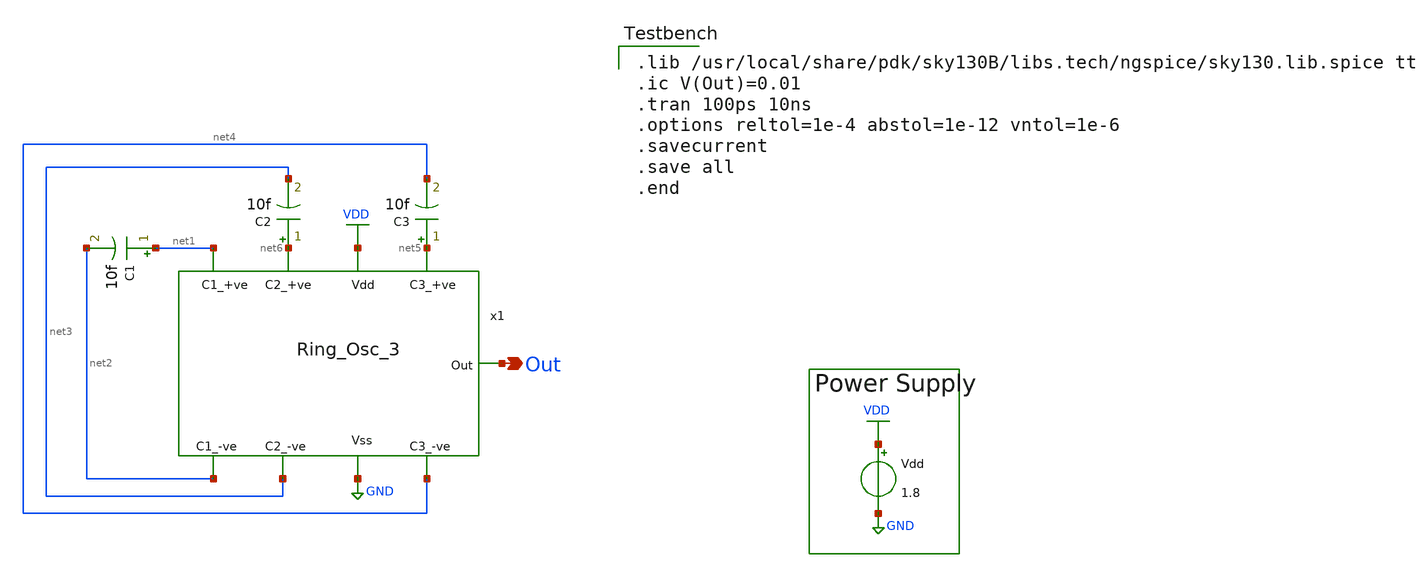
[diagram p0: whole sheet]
** sch_path: Xschem/RO_3_test.sch
**.subckt RO_3_test Out
*.opin Out
x1 VDD Out net5 net6 net1 net3 net4 net2 GND Ring_Osc_3
C1 net1 net2 10f m=1
C2 net6 net3 10f m=1
C3 net5 net4 10f m=1
Vdd VDD GND 1.8
**** begin user architecture code

.lib /usr/local/share/pdk/sky130B/libs.tech/ngspice/sky130.lib.spice tt
.ic V(Out)=0.01
.tran 100ps 10ns
.options reltol=1e-4 abstol=1e-12 vntol=1e-6
.savecurrent
.save all
.end

**** end user architecture code
**.ends

* expanding   symbol:  Ring_Osc_3.sym # of pins=9
** sym_path: Xschem/Ring_Osc_3.sym
** sch_path: Xschem/Ring_Osc_3.sch
.subckt Ring_Osc_3 Vdd Out C3_+ve C2_+ve C1_+ve C2_-ve C3_-ve C1_-ve Vss
*.opin Out
*.ipin Vss
*.ipin Vdd
*.ipin C1_-ve
*.ipin C1_+ve
*.ipin C2_-ve
*.ipin C2_+ve
*.ipin C3_+ve
*.ipin C3_-ve
x1 Vdd Out C1_+ve Vss inv
x2 Vdd C1_+ve C2_+ve Vss inv
x3 Vdd C2_+ve Out Vss inv
.ends


* expanding   symbol:  inv.sym # of pins=4
** sym_path: Xschem/inv.sym
** sch_path: Xschem/inv.sch
.subckt inv Vdd Vin Vout Vss
*.ipin Vin
*.ipin Vss
*.ipin Vdd
*.opin Vout
XM1 Vout Vin Vss GND sky130_fd_pr__nfet_01v8 L=0.15 W=1 nf=1 ad='int((nf+1)/2) * W/nf * 0.29' as='int((nf+2)/2) * W/nf * 0.29'
+ pd='2*int((nf+1)/2) * (W/nf + 0.29)' ps='2*int((nf+2)/2) * (W/nf + 0.29)' nrd='0.29 / W' nrs='0.29 / W'
+ sa=0 sb=0 sd=0 mult=1 m=1
XM2 Vout Vin Vdd VDD sky130_fd_pr__pfet_01v8 L=0.15 W=2.5 nf=1 ad='int((nf+1)/2) * W/nf * 0.29' as='int((nf+2)/2) * W/nf * 0.29'
+ pd='2*int((nf+1)/2) * (W/nf + 0.29)' ps='2*int((nf+2)/2) * (W/nf + 0.29)' nrd='0.29 / W' nrs='0.29 / W'
+ sa=0 sb=0 sd=0 mult=1 m=1
.ends

.GLOBAL GND
.GLOBAL VDD
.end
